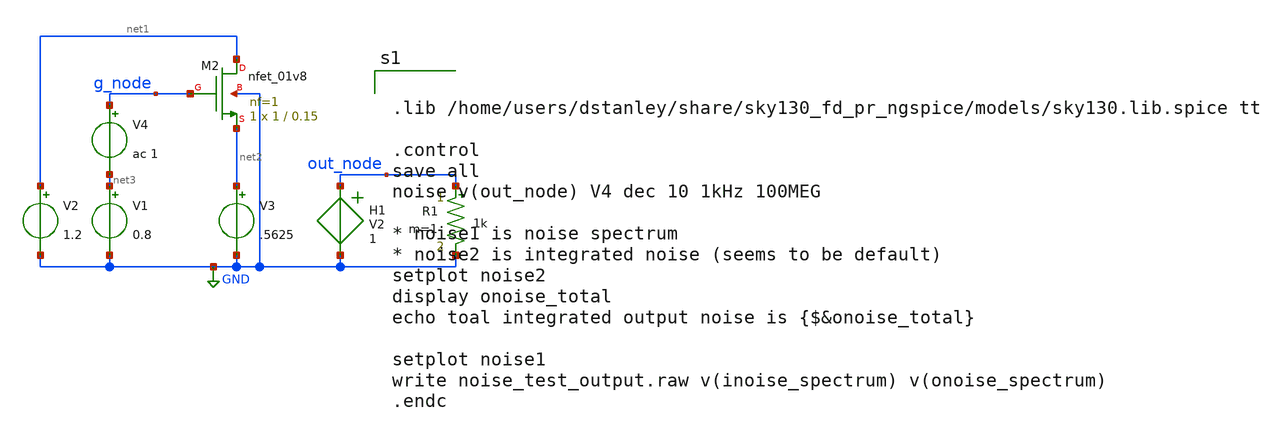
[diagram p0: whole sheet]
** sch_path: noise_test1.sch
**.subckt noise_test1
V1 net3 GND 0.8
V2 net1 GND 1.2
XM2 net1 g_node net2 GND sky130_fd_pr__nfet_01v8 L=0.15 W=1 nf=1 ad='int((nf+1)/2) * W/nf * 0.29' as='int((nf+2)/2) * W/nf * 0.29'
+ pd='2*int((nf+1)/2) * (W/nf + 0.29)' ps='2*int((nf+2)/2) * (W/nf + 0.29)' nrd='0.29 / W' nrs='0.29 / W'
+ sa=0 sb=0 sd=0 mult=1 m=1
V3 net2 GND .5625
H1 out_node GND V2 1
R1 out_node GND 1k m=1
V4 g_node net3 ac 1
**** begin user architecture code


.lib /home/users/dstanley/share/sky130_fd_pr_ngspice/models/sky130.lib.spice tt

.control
save all
noise v(out_node) V4 dec 10 1kHz 100MEG

* noise1 is noise spectrum
* noise2 is integrated noise (seems to be default)
setplot noise2
display onoise_total
echo toal integrated output noise is {$&onoise_total}

setplot noise1
write noise_test_output.raw v(inoise_spectrum) v(onoise_spectrum)
.endc


**** end user architecture code
**.ends
.GLOBAL GND
.end
